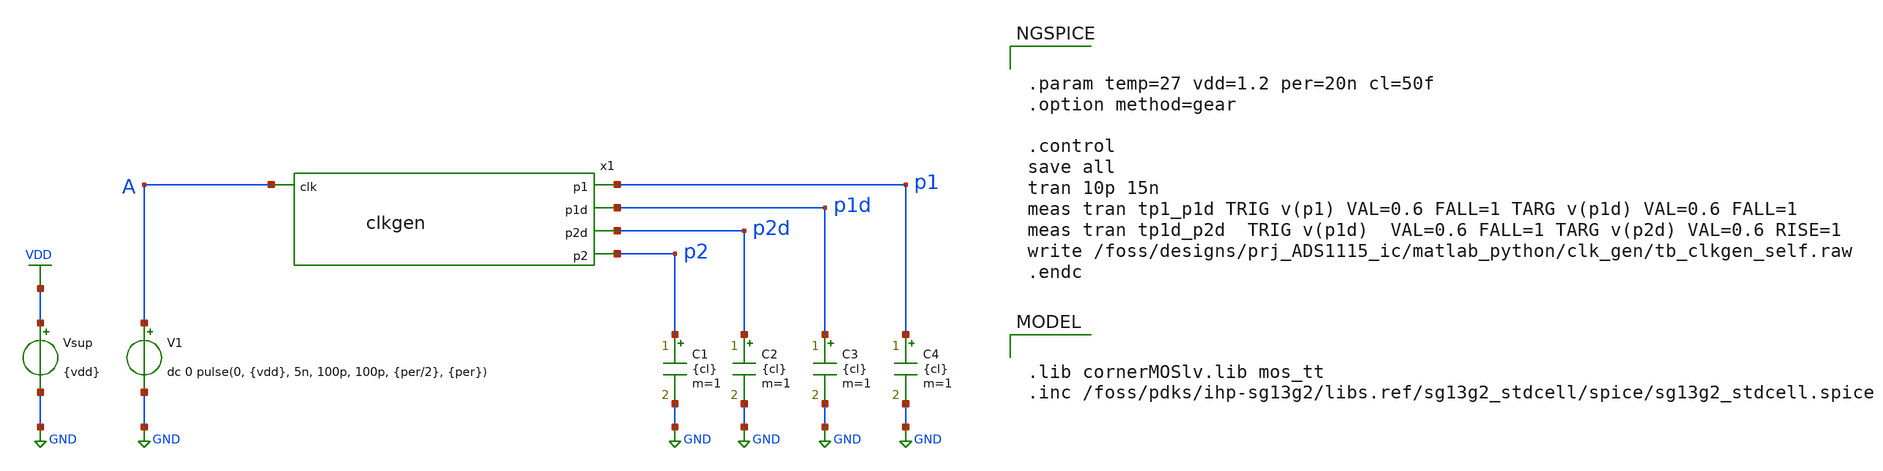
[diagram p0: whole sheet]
** sch_path: zip_meiners/ic_design/design_clkgen/tb_clkgen.sch
**.subckt tb_clkgen
V1 A GND dc 0 pulse(0, {vdd}, 5n, 100p, 100p, {per/2}, {per})
Vsup VDD GND {vdd}
C1 p2 GND {cl} m=1
C2 p2d GND {cl} m=1
C3 p1d GND {cl} m=1
C4 p1 GND {cl} m=1
x1 p1 p1d A p2d p2 clkgen
**** begin user architecture code

.lib cornerMOSlv.lib mos_tt
.inc /foss/pdks/ihp-sg13g2/libs.ref/sg13g2_stdcell/spice/sg13g2_stdcell.spice




.param temp=27 vdd=1.2 per=20n cl=50f
.option method=gear

.control
save all
tran 10p 15n
meas tran tp1_p1d TRIG v(p1) VAL=0.6 FALL=1 TARG v(p1d) VAL=0.6 FALL=1
meas tran tp1d_p2d  TRIG v(p1d)  VAL=0.6 FALL=1 TARG v(p2d) VAL=0.6 RISE=1
write /foss/designs/prj_ADS1115_ic/matlab_python/clk_gen/tb_clkgen_self.raw
.endc


**** end user architecture code
**.ends

* expanding   symbol:  /foss/designs/prj_ADS1115_ic/design/design_clkgen/clkgen.sym # of pins=5
** sym_path: design/design_clkgen/clkgen.sym
** sch_path: design/design_clkgen/clkgen.sch
.subckt clkgen p1 p1d clk p2d p2
*.ipin clk
*.opin p1
*.opin p1d
*.opin p2d
*.opin p2
x21 net6 net2 net11 VDD VSS sg13g2_nand2_1
x22 net1 clk VDD VSS sg13g2_inv_1
x2 net2 net1 VDD VSS sg13g2_inv_1
x8 net4 net5 VDD VSS sg13g2_inv_1
x9 net8 net4 VDD VSS sg13g2_inv_1
x10 net3 net6 VDD VSS sg13g2_inv_1
x11 net7 net3 VDD VSS sg13g2_inv_1
x12 p1 net7 VDD VSS sg13g2_inv_1
x14 p2 net8 VDD VSS sg13g2_inv_1
x16 net13 net16 VDD VSS sg13g2_inv_1
x18 p2d net13 VDD VSS sg13g2_inv_1
x19 net14 net15 VDD VSS sg13g2_inv_1
x20 p1d net14 VDD VSS sg13g2_inv_1
x4 net11 net12 VDD VSS sg13g2_inv_1
x17 net10 net9 VDD VSS sg13g2_inv_1
x1 net5 net10 net1 VDD VSS sg13g2_nand2_1
x23 net16 net12 net8 VDD VSS sg13g2_nand2_1
x24 net15 net7 net9 VDD VSS sg13g2_nand2_1
x29 net9 p1 VDD VSS sg13g2_inv_1
x30 net12 p2 VDD VSS sg13g2_inv_1
.ends


* expanding   symbol:  sg13g2_stdcells/sg13g2_nand2_1.sym # of pins=3
** sym_path: sg13g2_stdcells/sg13g2_nand2_1.sym
** sch_path: sg13g2_stdcells/sg13g2_nand2_1.sch
.subckt sg13g2_nand2_1 Y A B VDD VSS
*.iopin VDD
*.iopin VSS
*.ipin A
*.ipin B
*.opin Y
XM1 Y A net1 VSS sg13_lv_nmos w=740.00n l=130.00n ng=1 m=1 mm_ok=1
XM2 net1 B VSS VSS sg13_lv_nmos w=740.00n l=130.00n ng=1 m=1 mm_ok=1
XM3 Y A VDD VDD sg13_lv_pmos w=1.12u l=130.00n ng=1 m=1 mm_ok=1
XM4 Y B VDD VDD sg13_lv_pmos w=1.12u l=130.00n ng=1 m=1 mm_ok=1
.ends


* expanding   symbol:  sg13g2_stdcells/sg13g2_inv_1.sym # of pins=2
** sym_path: sg13g2_stdcells/sg13g2_inv_1.sym
** sch_path: sg13g2_stdcells/sg13g2_inv_1.sch
.subckt sg13g2_inv_1 Y A VDD VSS
*.opin Y
*.ipin A
*.iopin VDD
*.iopin VSS
XM1 Y A VSS VSS sg13_lv_nmos w=740.00n l=130.00n ng=1 m=1 mm_ok=1
XM2 Y A VDD VDD sg13_lv_pmos w=1.12u l=130.00n ng=1 m=1 mm_ok=1
.ends

.GLOBAL GND
.GLOBAL VDD
.end
